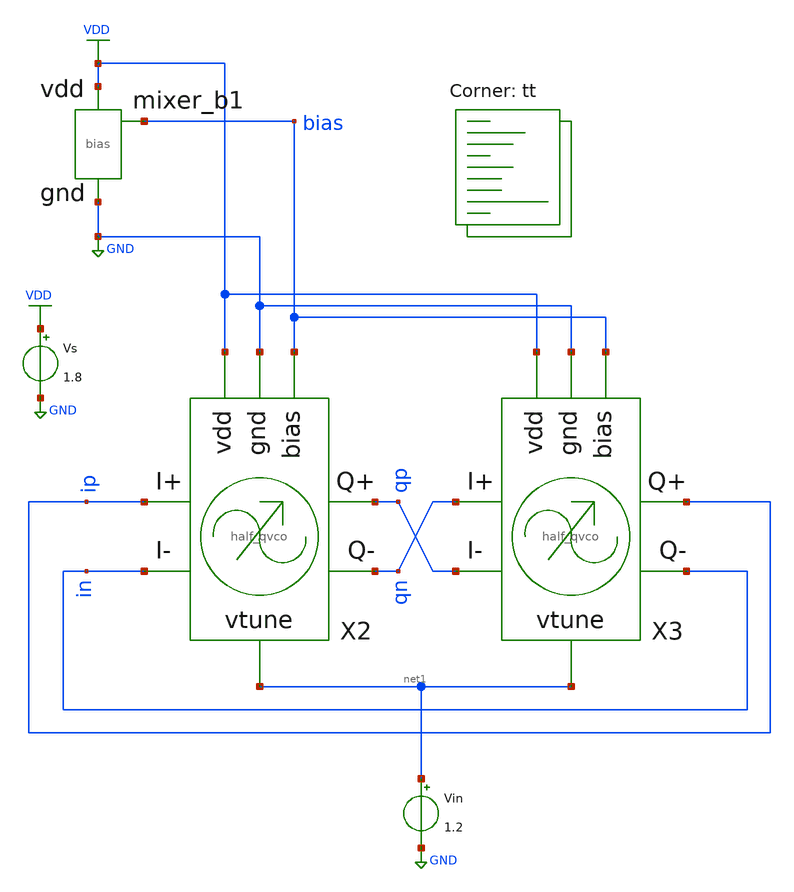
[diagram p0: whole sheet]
** sch_path: xschem/vco_transfer_tb.sch
**.subckt vco_transfer_tb
X2 VDD GND bias ip in qp qn net1 half_qvco
X3 VDD GND bias qn qp ip in net1 half_qvco
Vs VDD GND 1.8
Vin net1 GND 1.2
X1 bias VDD GND bias
**** begin user architecture code
.lib $::SKYWATER_MODELS/sky130.lib.spice tt


.control
tran 1p 50n
save all
write tb_transfer.raw
fft(v(qp))
plot mag(v(qp))
.endc


**** end user architecture code
**.ends
.GLOBAL GND
.GLOBAL VDD
.end
